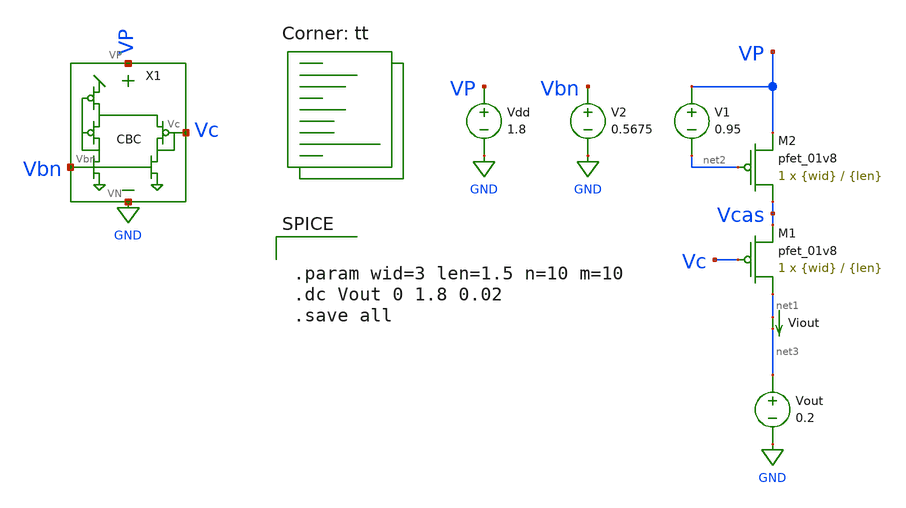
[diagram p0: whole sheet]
** sch_path: test_cbc.sch
**.subckt test_cbc
Vdd VP GND 1.8
V2 Vbn GND 0.5675
V1 VP net2 0.95
Viout net1 net3 0
.save i(viout)
Vout net3 GND 0.2
XM1 net1 Vc Vcas VP sky130_fd_pr__pfet_01v8 L={len} W={wid} nf=1 ad='int((nf+1)/2) * W/nf * 0.29' as='int((nf+2)/2) * W/nf * 0.29'
+ pd='2*int((nf+1)/2) * (W/nf + 0.29)' ps='2*int((nf+2)/2) * (W/nf + 0.29)' nrd='0.29 / W' nrs='0.29 / W'
+ sa=0 sb=0 sd=0 mult=1 m=1
XM2 Vcas net2 VP VP sky130_fd_pr__pfet_01v8 L={len} W={wid} nf=1 ad='int((nf+1)/2) * W/nf * 0.29' as='int((nf+2)/2) * W/nf * 0.29'
+ pd='2*int((nf+1)/2) * (W/nf + 0.29)' ps='2*int((nf+2)/2) * (W/nf + 0.29)' nrd='0.29 / W' nrs='0.29 / W'
+ sa=0 sb=0 sd=0 mult=1 m=1
X1 Vbn Vc VP GND cbc
**** begin user architecture code


.param wid=3 len=1.5 n=10 m=10
.dc Vout 0 1.8 0.02
.save all


.lib $::SKYWATER_MODELS/sky130.lib.spice tt
**** end user architecture code
**.ends

* expanding   symbol:  cbc.sym # of pins=4
** sym_path: cbc.sym
** sch_path: cbc.sch
.subckt cbc Vbn Vc VP VN
*.iopin VP
*.iopin VN
*.opin Vc
*.ipin Vbn
XM8 Vbg Vbg Vdssat VP sky130_fd_pr__pfet_01v8 L={cbc_len} W={cbc_wid}*{m} nf=1 ad='int((nf+1)/2) * W/nf * 0.29'
+ as='int((nf+2)/2) * W/nf * 0.29' pd='2*int((nf+1)/2) * (W/nf + 0.29)' ps='2*int((nf+2)/2) * (W/nf + 0.29)'
+ nrd='0.29 / W' nrs='0.29 / W' sa=0 sb=0 sd=0 mult=1 m=1
XM9 Vbg Vbn VN VN sky130_fd_pr__nfet_01v8 L={cbc_len}*{n} W={cbc_wid} nf=1 ad='int((nf+1)/2) * W/nf * 0.29'
+ as='int((nf+2)/2) * W/nf * 0.29' pd='2*int((nf+1)/2) * (W/nf + 0.29)' ps='2*int((nf+2)/2) * (W/nf + 0.29)'
+ nrd='0.29 / W' nrs='0.29 / W' sa=0 sb=0 sd=0 mult=1 m=1
XM10 Vc Vbn VN VN sky130_fd_pr__nfet_01v8 L={cbc_len} W={cbc_wid} nf=1 ad='int((nf+1)/2) * W/nf * 0.29'
+ as='int((nf+2)/2) * W/nf * 0.29' pd='2*int((nf+1)/2) * (W/nf + 0.29)' ps='2*int((nf+2)/2) * (W/nf + 0.29)'
+ nrd='0.29 / W' nrs='0.29 / W' sa=0 sb=0 sd=0 mult=1 m=1
XM11 Vdssat Vbg VP VP sky130_fd_pr__pfet_01v8 L={cbc_len} W={cbc_wid} nf=1 ad='int((nf+1)/2) * W/nf * 0.29'
+ as='int((nf+2)/2) * W/nf * 0.29' pd='2*int((nf+1)/2) * (W/nf + 0.29)' ps='2*int((nf+2)/2) * (W/nf + 0.29)'
+ nrd='0.29 / W' nrs='0.29 / W' sa=0 sb=0 sd=0 mult=1 m=1
XM12 Vdssat Vc Vc VP sky130_fd_pr__pfet_01v8 L={cbc_len} W={cbc_wid} nf=1 ad='int((nf+1)/2) * W/nf * 0.29'
+ as='int((nf+2)/2) * W/nf * 0.29' pd='2*int((nf+1)/2) * (W/nf + 0.29)' ps='2*int((nf+2)/2) * (W/nf + 0.29)'
+ nrd='0.29 / W' nrs='0.29 / W' sa=0 sb=0 sd=0 mult=1 m=1
**** begin user architecture code


.param cbc_wid=3 cbc_len=1.5 n=10 m=10


**** end user architecture code
.ends

.GLOBAL GND
.end
